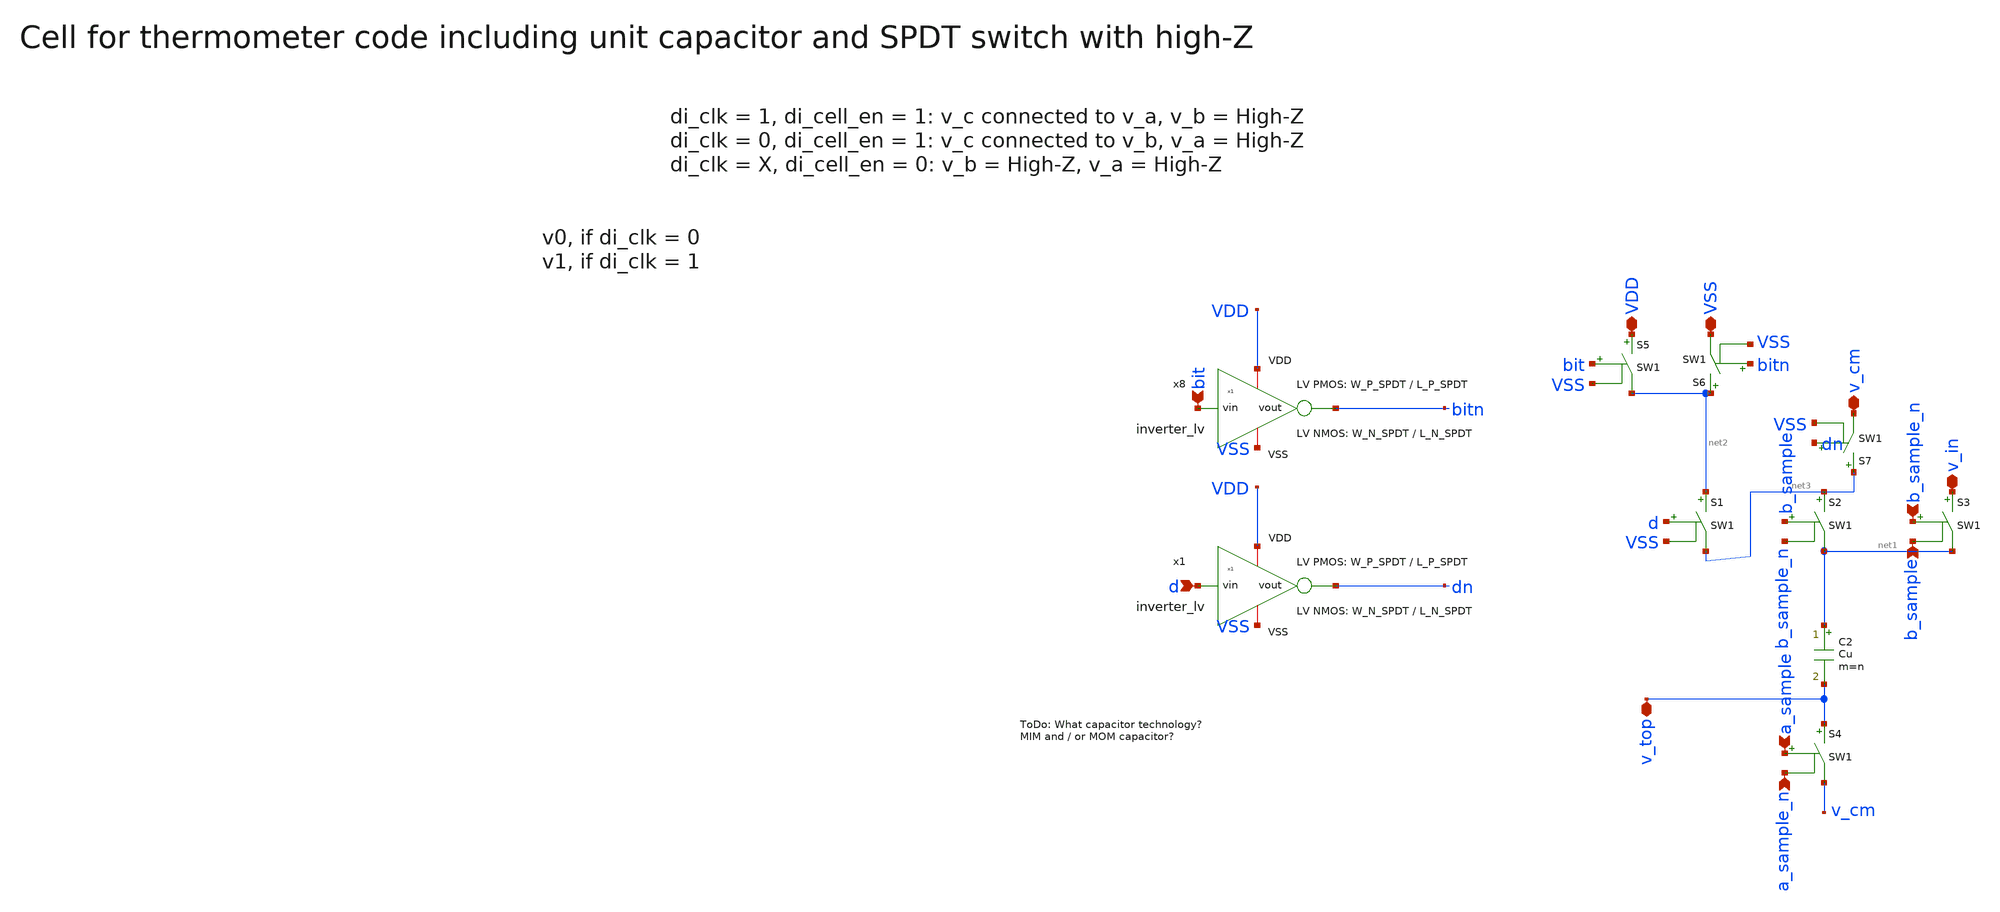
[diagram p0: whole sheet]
** sch_path: xschem/dac_icms_cell/unit_cell_n.sch
**.subckt unit_cell_n VSS v_in d bit v_top v_cm b_sample b_sample_n a_sample a_sample_n VDD
*.iopin VSS
*.iopin v_in
*.ipin d
*.ipin bit
*.iopin v_top
*.iopin v_cm
*.ipin b_sample
*.ipin b_sample_n
*.ipin a_sample
*.ipin a_sample_n
*.iopin VDD
S1 net2 net3 d VSS SW1
C2 net1 v_top Cu m=n
S2 net3 net1 b_sample b_sample_n SW1
S3 v_in net1 b_sample_n b_sample SW1
S4 v_top v_cm a_sample a_sample_n SW1
S5 VDD net2 bit VSS SW1
S6 net2 VSS bitn VSS SW1
S7 net3 v_cm dn VSS SW1
x8 VDD bit bitn VSS inverter_lv W_P=W_P_SPDT L_P=L_P_SPDT W_N=W_N_SPDT L_N=L_N_SPDT N_C=1
x1 VDD d dn VSS inverter_lv W_P=W_P_SPDT L_P=L_P_SPDT W_N=W_N_SPDT L_N=L_N_SPDT N_C=1
**.ends

* expanding   symbol:  inverter/inverter_lv.sym # of pins=4
** sym_path: xschem/inverter/inverter_lv.sym
** sch_path: xschem/inverter/inverter_lv.sch
.subckt inverter_lv VDD vin vout VSS  W_P=3.0u L_P=0.13u W_N=1.0u L_N=0.13u N_C=1
*.ipin vin
*.iopin VDD
*.iopin VSS
*.opin vout
XM1 vout vin VDD VDD sg13_lv_pmos w=W_P l=L_P ng=1 m={N_C} mm_ok=1
XM2 vout vin VSS VSS sg13_lv_nmos w=W_N l=L_N ng=1 m={N_C} mm_ok=1
.ends

**** begin user architecture code
.MODEL SW1 SW   VT=0.9 VH=0.01  RON= {ro/2} ROFF=10G
**** end user architecture code
.end
